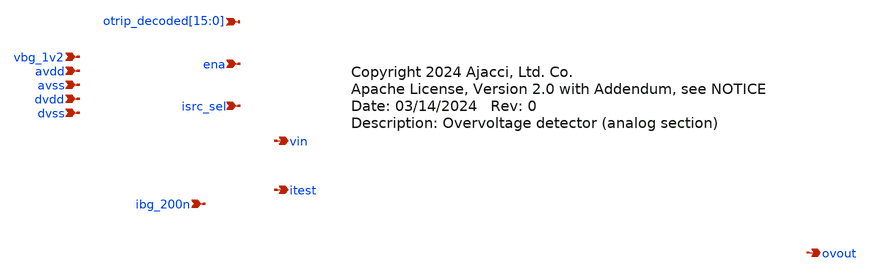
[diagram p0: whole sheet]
** sch_path: xschem/overvoltage_ana_rcx.sch
* Copyright 2024 Ajacci, Ltd. Co.
* Apache License, Version 2.0 with Addendum, see NOTICE
**.subckt overvoltage_ana_rcx vbg_1v2 avdd avss dvdd dvss ena isrc_sel ibg_200n ovout itest
*+ otrip_decoded[15],otrip_decoded[14],otrip_decoded[13],otrip_decoded[12],otrip_decoded[11],otrip_decoded[10],otrip_decoded[9],otrip_decoded[8],otrip_decoded[7],otrip_decoded[6],otrip_decoded[5],otrip_decoded[4],otrip_decoded[3],otrip_decoded[2],otrip_decoded[1],otrip_decoded[0] vin
*.ipin vbg_1v2
*.ipin avdd
*.ipin avss
*.ipin dvdd
*.ipin dvss
*.ipin ena
*.ipin isrc_sel
*.ipin ibg_200n
*.opin ovout
*.opin itest
*.ipin
*+ otrip_decoded[15],otrip_decoded[14],otrip_decoded[13],otrip_decoded[12],otrip_decoded[11],otrip_decoded[10],otrip_decoded[9],otrip_decoded[8],otrip_decoded[7],otrip_decoded[6],otrip_decoded[5],otrip_decoded[4],otrip_decoded[3],otrip_decoded[2],otrip_decoded[1],otrip_decoded[0]
*.opin vin
**** begin user architecture code



.include mag/rcx/overvoltage_ana_rcx.spice

xIana otrip_decoded[14] otrip_decoded[13] otrip_decoded[11]  otrip_decoded[10] otrip_decoded[1]
+ otrip_decoded[0] ena itest ibg_200n otrip_decoded[7]  otrip_decoded[4] vbg_1v2 vin isrc_sel otrip_decoded[5]
+ otrip_decoded[8] otrip_decoded[2]  ovout otrip_decoded[15] otrip_decoded[9] otrip_decoded[12] otrip_decoded[3]
+ otrip_decoded[6]  avss dvdd dvss avdd overvoltage_ana_rcx


**** end user architecture code
**.ends
.end
